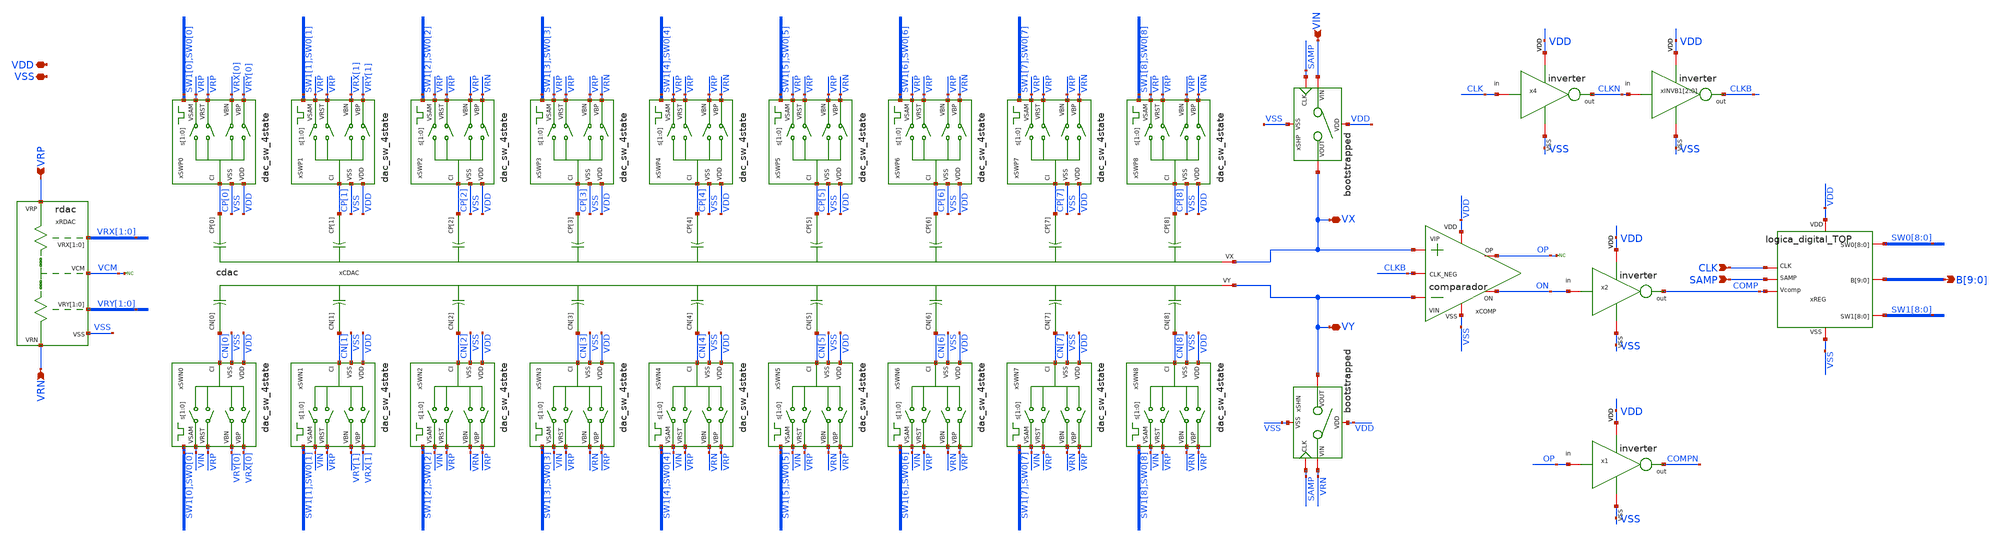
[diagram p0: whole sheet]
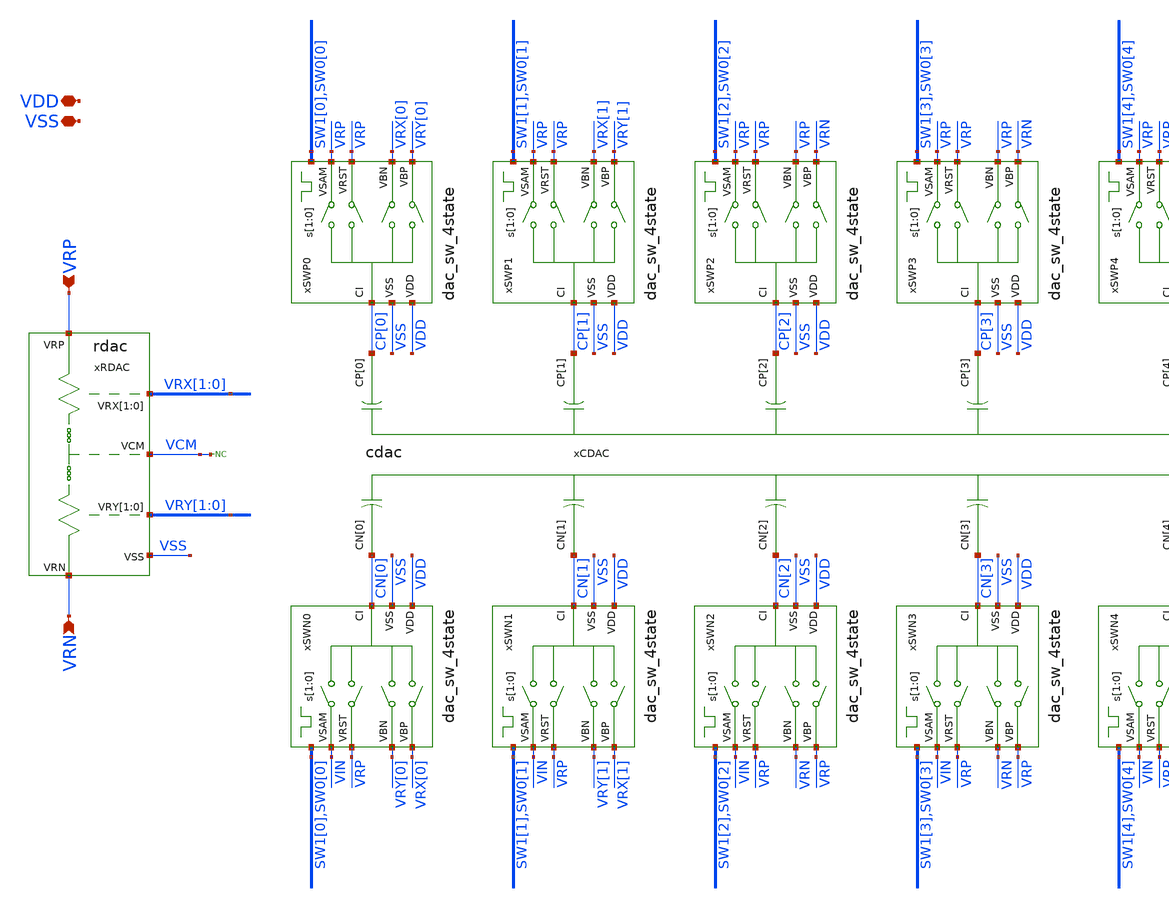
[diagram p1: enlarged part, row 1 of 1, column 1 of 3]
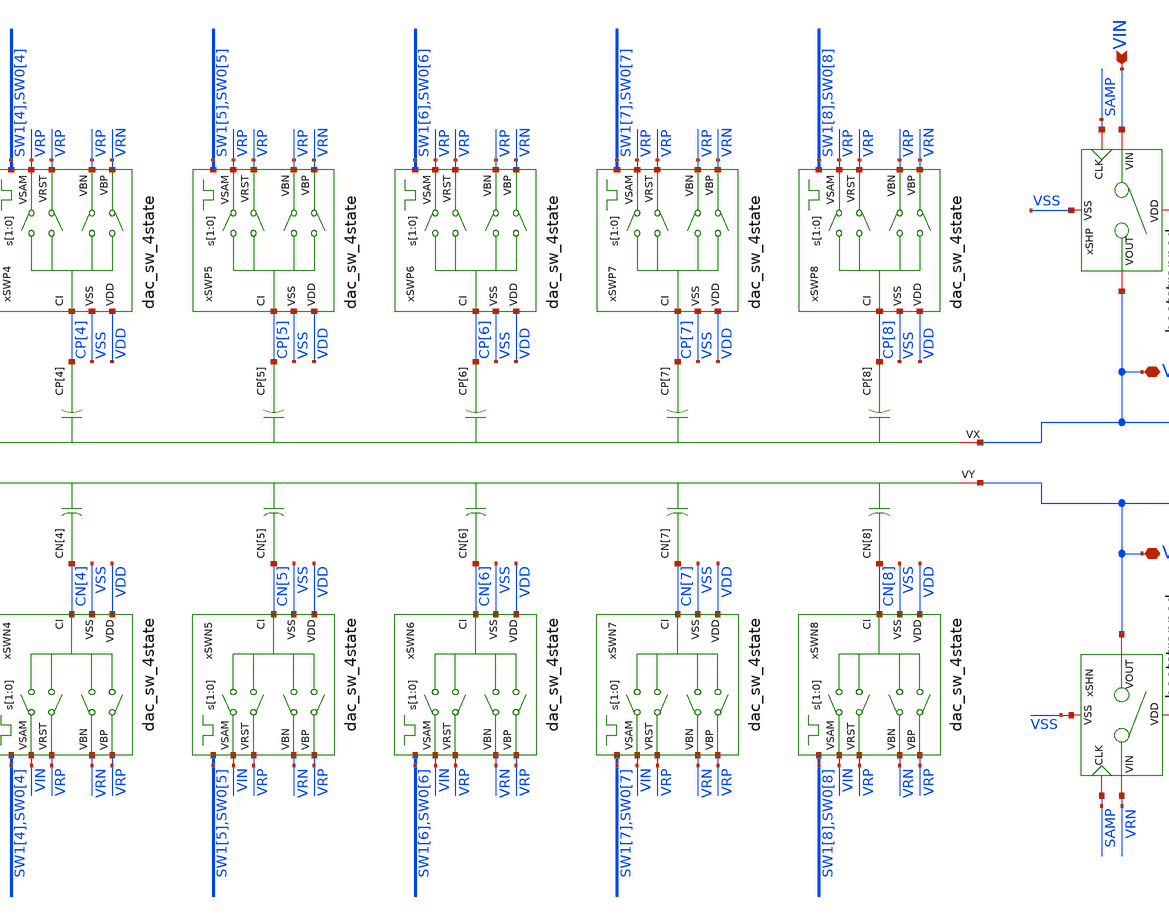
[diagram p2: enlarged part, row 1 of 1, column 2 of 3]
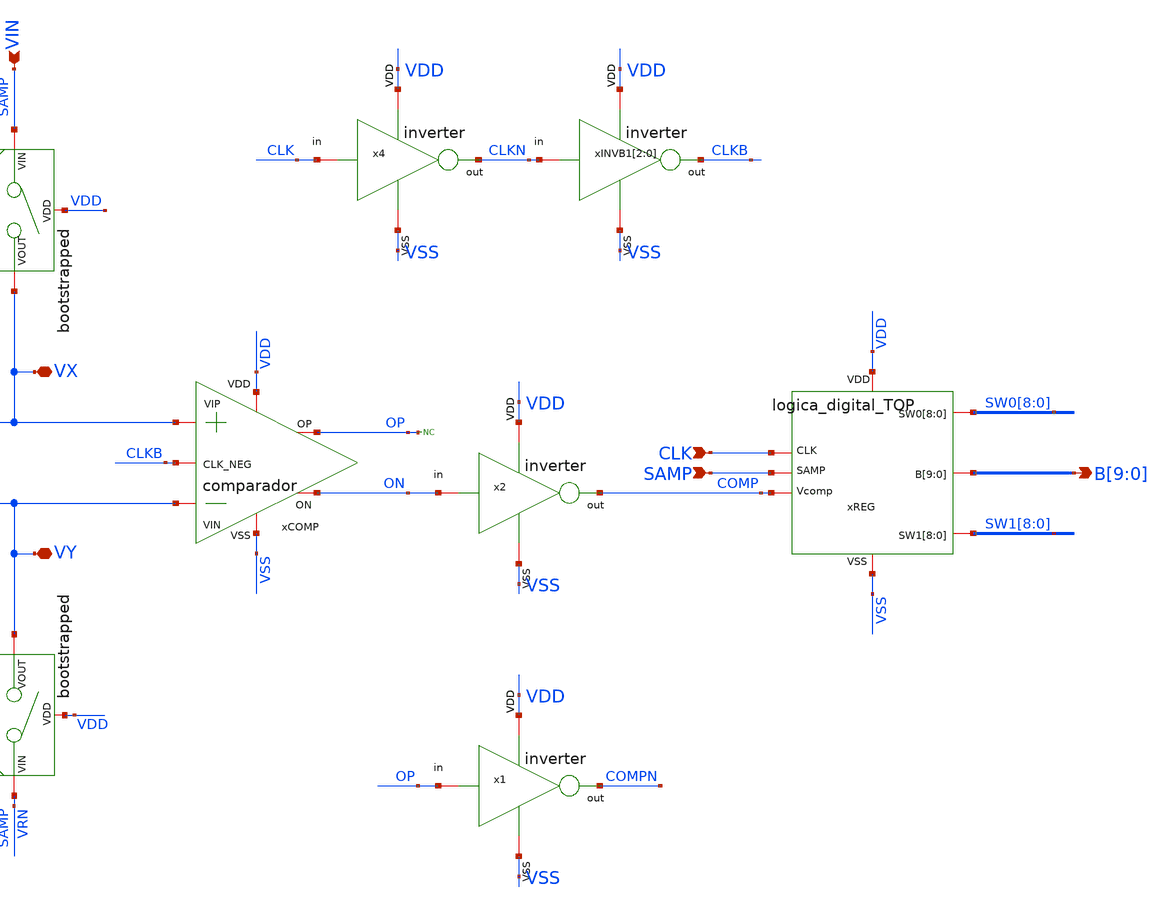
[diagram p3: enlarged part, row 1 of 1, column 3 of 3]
** sch_path: designs/sar_adc/top/sar_adc_10b/xschem/sar_adc_10b.sch
**.subckt sar_adc_10b VSS VDD VRP VRN CLK SAMP B[9],B[8],B[7],B[6],B[5],B[4],B[3],B[2],B[1],B[0] VIN
*+ VY VX
*.iopin VSS
*.iopin VDD
*.ipin VRP
*.ipin VRN
*.ipin CLK
*.ipin SAMP
*.opin B[9],B[8],B[7],B[6],B[5],B[4],B[3],B[2],B[1],B[0]
*.ipin VIN
*.iopin VY
*.iopin VX
xCDAC CP[8] CP[3] CP[5] CP[1] CP[0] CP[4] CP[6] CP[7] CP[2] CN[2] CN[1] CN[3] CN[8] CN[7] CN[6]
+ CN[5] CN[4] CN[0] VX VY cdac
xRDAC VCM VRX[1] VRX[0] VRY[1] VRY[0] VRP VRN VSS rdac
xSWP0 VDD SW1[0] SW0[0] VSS CP[0] VRP VRY[0] VRX[0] VRP dac_sw_4state
xSWP1 VDD SW1[1] SW0[1] VSS CP[1] VRP VRY[1] VRX[1] VRP dac_sw_4state
xSWP2 VDD SW1[2] SW0[2] VSS CP[2] VRP VRN VRP VRP dac_sw_4state
xSWP3 VDD SW1[3] SW0[3] VSS CP[3] VRP VRN VRP VRP dac_sw_4state
xSWP4 VDD SW1[4] SW0[4] VSS CP[4] VRP VRN VRP VRP dac_sw_4state
xSWP5 VDD SW1[5] SW0[5] VSS CP[5] VRP VRN VRP VRP dac_sw_4state
xSWP6 VDD SW1[6] SW0[6] VSS CP[6] VRP VRN VRP VRP dac_sw_4state
xSWP7 VDD SW1[7] SW0[7] VSS CP[7] VRP VRN VRP VRP dac_sw_4state
xSWP8 VDD SW1[8] SW0[8] VSS CP[8] VRP VRN VRP VRP dac_sw_4state
xSWN0 VDD SW1[0] SW0[0] VSS CN[0] VIN VRX[0] VRY[0] VRP dac_sw_4state
xSWN1 VDD SW1[1] SW0[1] VSS CN[1] VIN VRX[1] VRY[1] VRP dac_sw_4state
xSWN2 VDD SW1[2] SW0[2] VSS CN[2] VIN VRP VRN VRP dac_sw_4state
xSWN3 VDD SW1[3] SW0[3] VSS CN[3] VIN VRP VRN VRP dac_sw_4state
xSWN4 VDD SW1[4] SW0[4] VSS CN[4] VIN VRP VRN VRP dac_sw_4state
xSWN5 VDD SW1[5] SW0[5] VSS CN[5] VIN VRP VRN VRP dac_sw_4state
xSWN6 VDD SW1[6] SW0[6] VSS CN[6] VIN VRP VRN VRP dac_sw_4state
xSWN7 VDD SW1[7] SW0[7] VSS CN[7] VIN VRP VRN VRP dac_sw_4state
xSWN8 VDD SW1[8] SW0[8] VSS CN[8] VIN VRP VRN VRP dac_sw_4state
* noconn VCM
xCOMP VDD CLKB ON OP VY VX VSS comparador
* noconn OP
xSHP VDD VSS SAMP VIN VX bootstrapped
xSHN VDD VSS SAMP VRN VY bootstrapped
xREG VDD CLK SAMP COMP SW0[8] SW0[7] SW0[6] SW0[5] SW0[4] SW0[3] SW0[2] SW0[1] SW0[0] B[9] B[8] B[7]
+ B[6] B[5] B[4] B[3] B[2] B[1] B[0] SW1[8] SW1[7] SW1[6] SW1[5] SW1[4] SW1[3] SW1[2] SW1[1] SW1[0] VSS
+ logica_digital_TOP
x2 VDD ON COMP VSS inverter
x4 VDD CLK CLKN VSS inverter
xINVB1[2] VDD CLKN CLKB VSS inverter
xINVB1[1] VDD CLKN CLKB VSS inverter
xINVB1[0] VDD CLKN CLKB VSS inverter
x1 VDD OP COMPN VSS inverter
**.ends
.end
